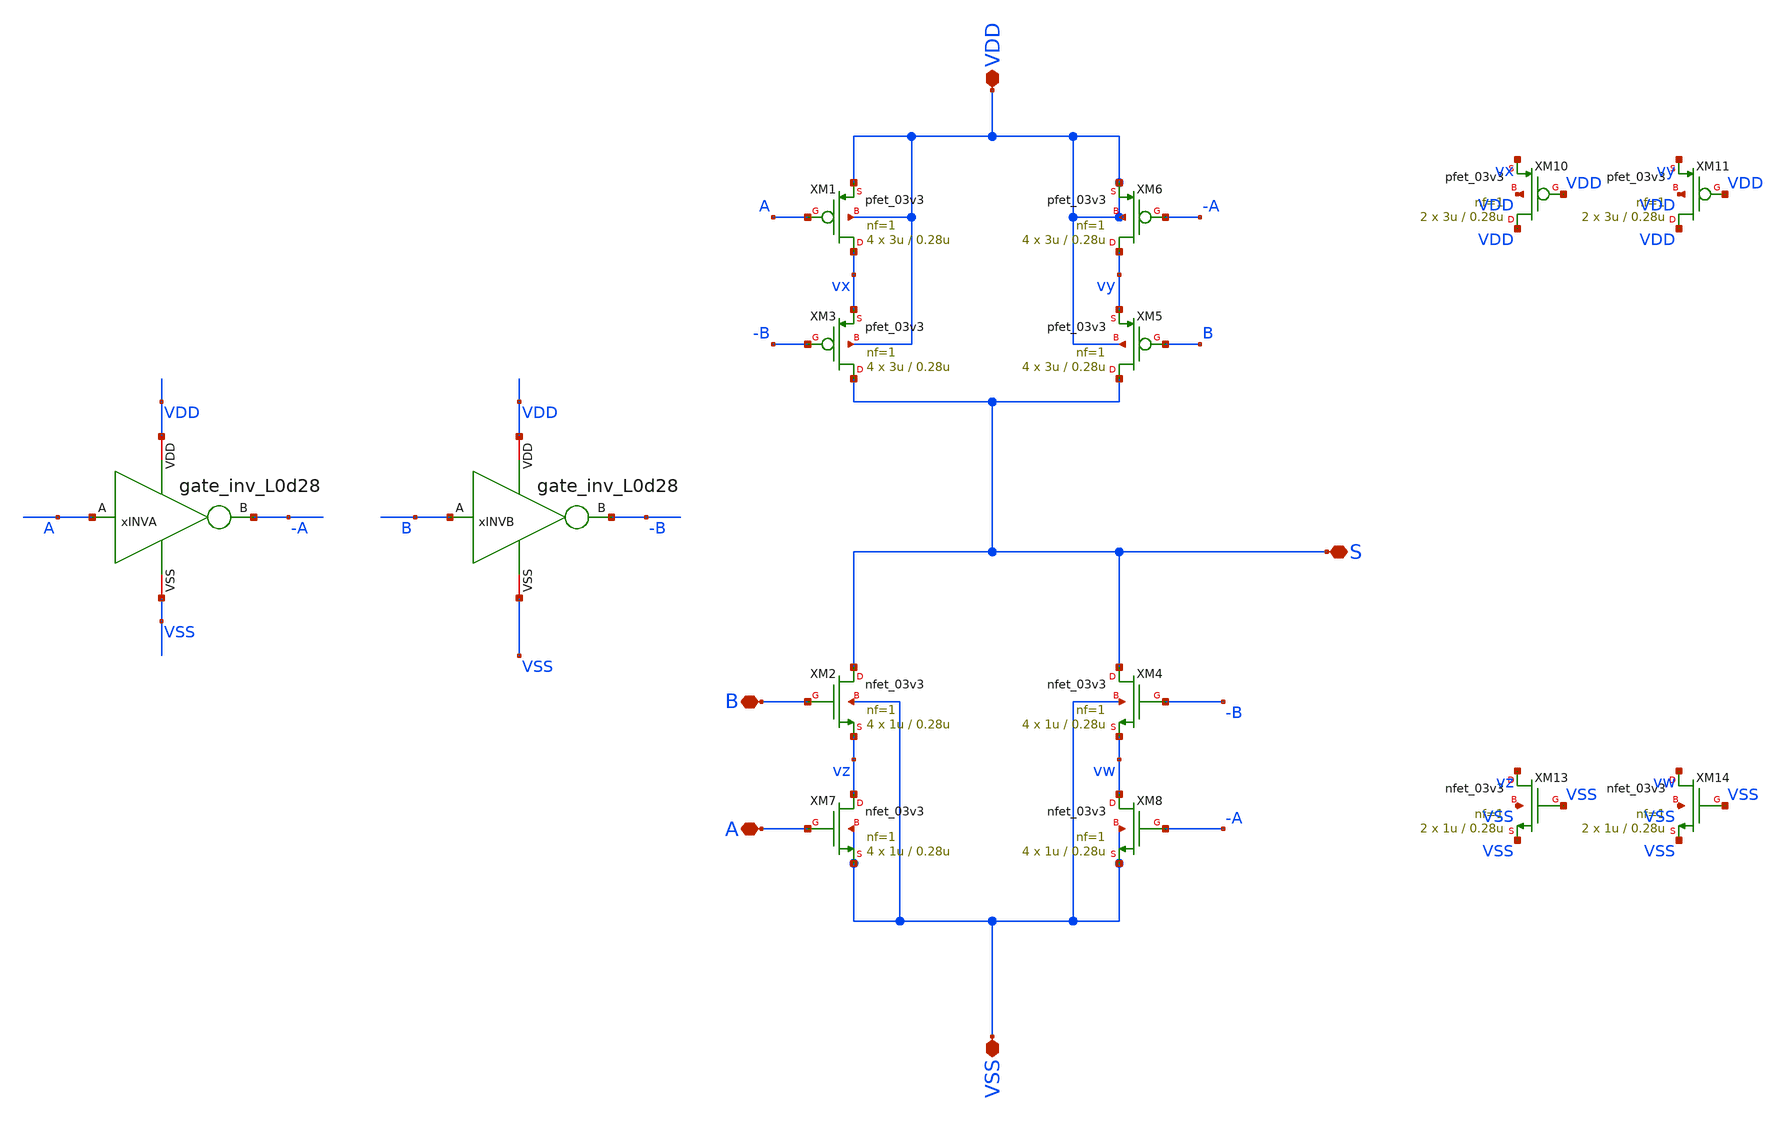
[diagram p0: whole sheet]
** sch_path: designs/DS_modulator/gate_xor/xschem/gate_xor.sch
**.subckt gate_xor VSS VDD S A B
*.iopin VSS
*.iopin VDD
*.iopin S
*.iopin A
*.iopin B
XM2 S B vz VSS nfet_03v3 L=0.28u W=1u nf=1 ad='int((nf+1)/2) * W/nf * 0.18u' as='int((nf+2)/2) * W/nf * 0.18u'
+ pd='2*int((nf+1)/2) * (W/nf + 0.18u)' ps='2*int((nf+2)/2) * (W/nf + 0.18u)' nrd='0.18u / W' nrs='0.18u / W'
+ sa=0 sb=0 sd=0 m=4
XM3 S -B vx VDD pfet_03v3 L=0.28u W=3u nf=1 ad='int((nf+1)/2) * W/nf * 0.18u' as='int((nf+2)/2) * W/nf * 0.18u'
+ pd='2*int((nf+1)/2) * (W/nf + 0.18u)' ps='2*int((nf+2)/2) * (W/nf + 0.18u)' nrd='0.18u / W' nrs='0.18u / W'
+ sa=0 sb=0 sd=0 m=4
XM1 vx A VDD VDD pfet_03v3 L=0.28u W=3u nf=1 ad='int((nf+1)/2) * W/nf * 0.18u' as='int((nf+2)/2) * W/nf * 0.18u'
+ pd='2*int((nf+1)/2) * (W/nf + 0.18u)' ps='2*int((nf+2)/2) * (W/nf + 0.18u)' nrd='0.18u / W' nrs='0.18u / W'
+ sa=0 sb=0 sd=0 m=4
XM4 S -B vw VSS nfet_03v3 L=0.28u W=1u nf=1 ad='int((nf+1)/2) * W/nf * 0.18u' as='int((nf+2)/2) * W/nf * 0.18u'
+ pd='2*int((nf+1)/2) * (W/nf + 0.18u)' ps='2*int((nf+2)/2) * (W/nf + 0.18u)' nrd='0.18u / W' nrs='0.18u / W'
+ sa=0 sb=0 sd=0 m=4
XM5 S B vy VDD pfet_03v3 L=0.28u W=3u nf=1 ad='int((nf+1)/2) * W/nf * 0.18u' as='int((nf+2)/2) * W/nf * 0.18u'
+ pd='2*int((nf+1)/2) * (W/nf + 0.18u)' ps='2*int((nf+2)/2) * (W/nf + 0.18u)' nrd='0.18u / W' nrs='0.18u / W'
+ sa=0 sb=0 sd=0 m=4
XM6 vy -A VDD VDD pfet_03v3 L=0.28u W=3u nf=1 ad='int((nf+1)/2) * W/nf * 0.18u' as='int((nf+2)/2) * W/nf * 0.18u'
+ pd='2*int((nf+1)/2) * (W/nf + 0.18u)' ps='2*int((nf+2)/2) * (W/nf + 0.18u)' nrd='0.18u / W' nrs='0.18u / W'
+ sa=0 sb=0 sd=0 m=4
XM7 vz A VSS VSS nfet_03v3 L=0.28u W=1u nf=1 ad='int((nf+1)/2) * W/nf * 0.18u' as='int((nf+2)/2) * W/nf * 0.18u'
+ pd='2*int((nf+1)/2) * (W/nf + 0.18u)' ps='2*int((nf+2)/2) * (W/nf + 0.18u)' nrd='0.18u / W' nrs='0.18u / W'
+ sa=0 sb=0 sd=0 m=4
XM8 vw -A VSS VSS nfet_03v3 L=0.28u W=1u nf=1 ad='int((nf+1)/2) * W/nf * 0.18u' as='int((nf+2)/2) * W/nf * 0.18u'
+ pd='2*int((nf+1)/2) * (W/nf + 0.18u)' ps='2*int((nf+2)/2) * (W/nf + 0.18u)' nrd='0.18u / W' nrs='0.18u / W'
+ sa=0 sb=0 sd=0 m=4
xINVA VDD -A A VSS gate_inv_L0d28
xINVB VDD -B B VSS gate_inv_L0d28
XM10 VDD VDD vx VDD pfet_03v3 L=0.28u W=3u nf=1 ad='int((nf+1)/2) * W/nf * 0.18u' as='int((nf+2)/2) * W/nf * 0.18u'
+ pd='2*int((nf+1)/2) * (W/nf + 0.18u)' ps='2*int((nf+2)/2) * (W/nf + 0.18u)' nrd='0.18u / W' nrs='0.18u / W'
+ sa=0 sb=0 sd=0 m=2
XM11 VDD VDD vy VDD pfet_03v3 L=0.28u W=3u nf=1 ad='int((nf+1)/2) * W/nf * 0.18u' as='int((nf+2)/2) * W/nf * 0.18u'
+ pd='2*int((nf+1)/2) * (W/nf + 0.18u)' ps='2*int((nf+2)/2) * (W/nf + 0.18u)' nrd='0.18u / W' nrs='0.18u / W'
+ sa=0 sb=0 sd=0 m=2
XM13 vz VSS VSS VSS nfet_03v3 L=0.28u W=1u nf=1 ad='int((nf+1)/2) * W/nf * 0.18u' as='int((nf+2)/2) * W/nf * 0.18u'
+ pd='2*int((nf+1)/2) * (W/nf + 0.18u)' ps='2*int((nf+2)/2) * (W/nf + 0.18u)' nrd='0.18u / W' nrs='0.18u / W'
+ sa=0 sb=0 sd=0 m=2
XM14 vw VSS VSS VSS nfet_03v3 L=0.28u W=1u nf=1 ad='int((nf+1)/2) * W/nf * 0.18u' as='int((nf+2)/2) * W/nf * 0.18u'
+ pd='2*int((nf+1)/2) * (W/nf + 0.18u)' ps='2*int((nf+2)/2) * (W/nf + 0.18u)' nrd='0.18u / W' nrs='0.18u / W'
+ sa=0 sb=0 sd=0 m=2
**.ends

* expanding   symbol:
*+  /foss/designs/chipathon_2025/designs/gf180/gate_inv_L0d28/xschem/gate_inv_L0d28.sym # of pins=4
** sym_path: designs/DS_modulator/gate_inv_L0d28/xschem/gate_inv_L0d28.sym
** sch_path: designs/DS_modulator/gate_inv_L0d28/xschem/gate_inv_L0d28.sch
.subckt gate_inv_L0d28 VDD B A VSS
*.opin B
*.ipin A
*.iopin VDD
*.iopin VSS
XMN B A VSS VSS nfet_03v3 L=0.28u W=1u nf=1 ad='int((nf+1)/2) * W/nf * 0.18u' as='int((nf+2)/2) * W/nf * 0.18u'
+ pd='2*int((nf+1)/2) * (W/nf + 0.18u)' ps='2*int((nf+2)/2) * (W/nf + 0.18u)' nrd='0.18u / W' nrs='0.18u / W'
+ sa=0 sb=0 sd=0 m=2
XMP B A VDD VDD pfet_03v3 L=0.28u W=3u nf=1 ad='int((nf+1)/2) * W/nf * 0.18u' as='int((nf+2)/2) * W/nf * 0.18u'
+ pd='2*int((nf+1)/2) * (W/nf + 0.18u)' ps='2*int((nf+2)/2) * (W/nf + 0.18u)' nrd='0.18u / W' nrs='0.18u / W'
+ sa=0 sb=0 sd=0 m=2
.ends

.end
